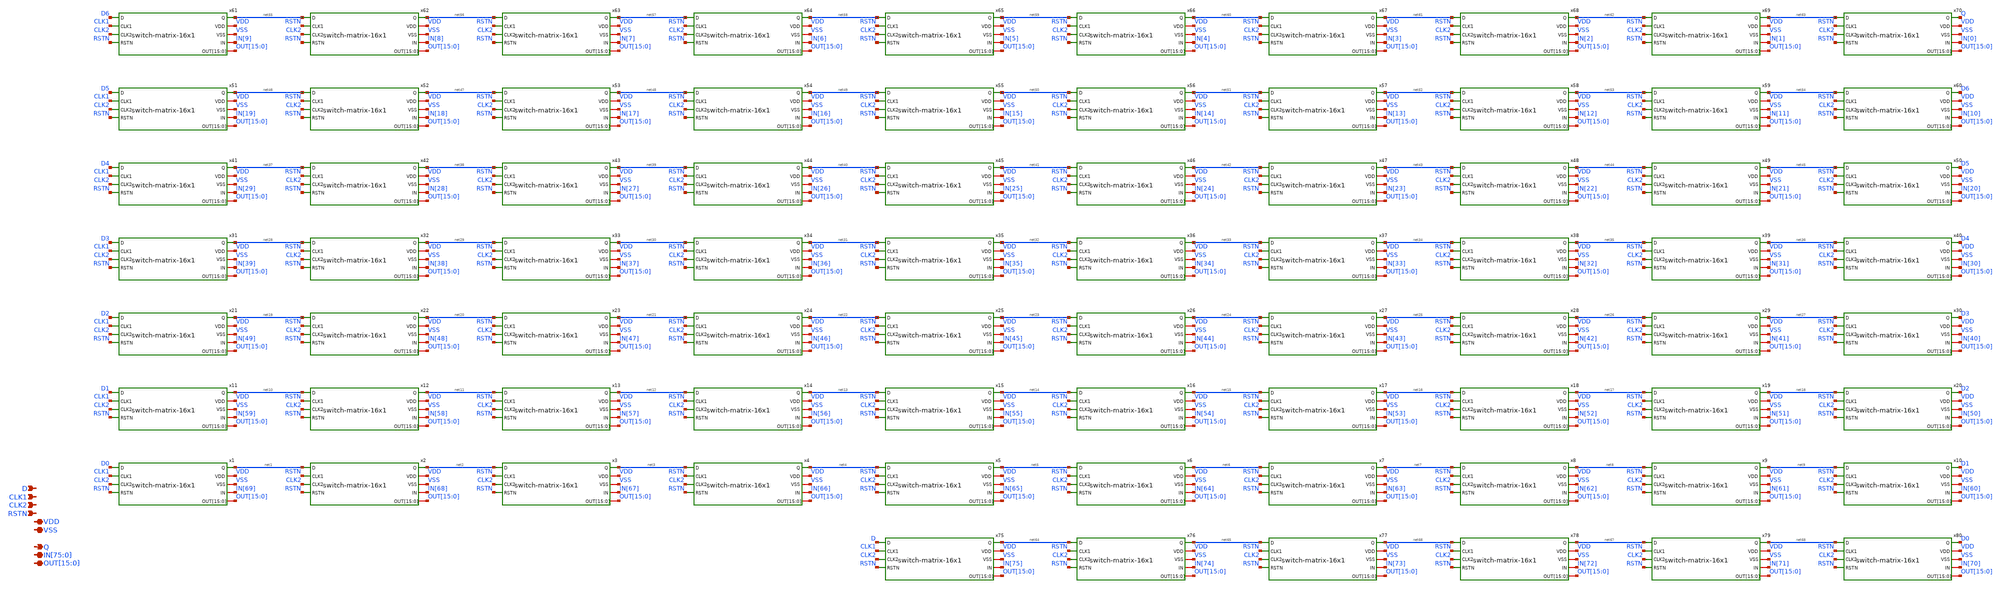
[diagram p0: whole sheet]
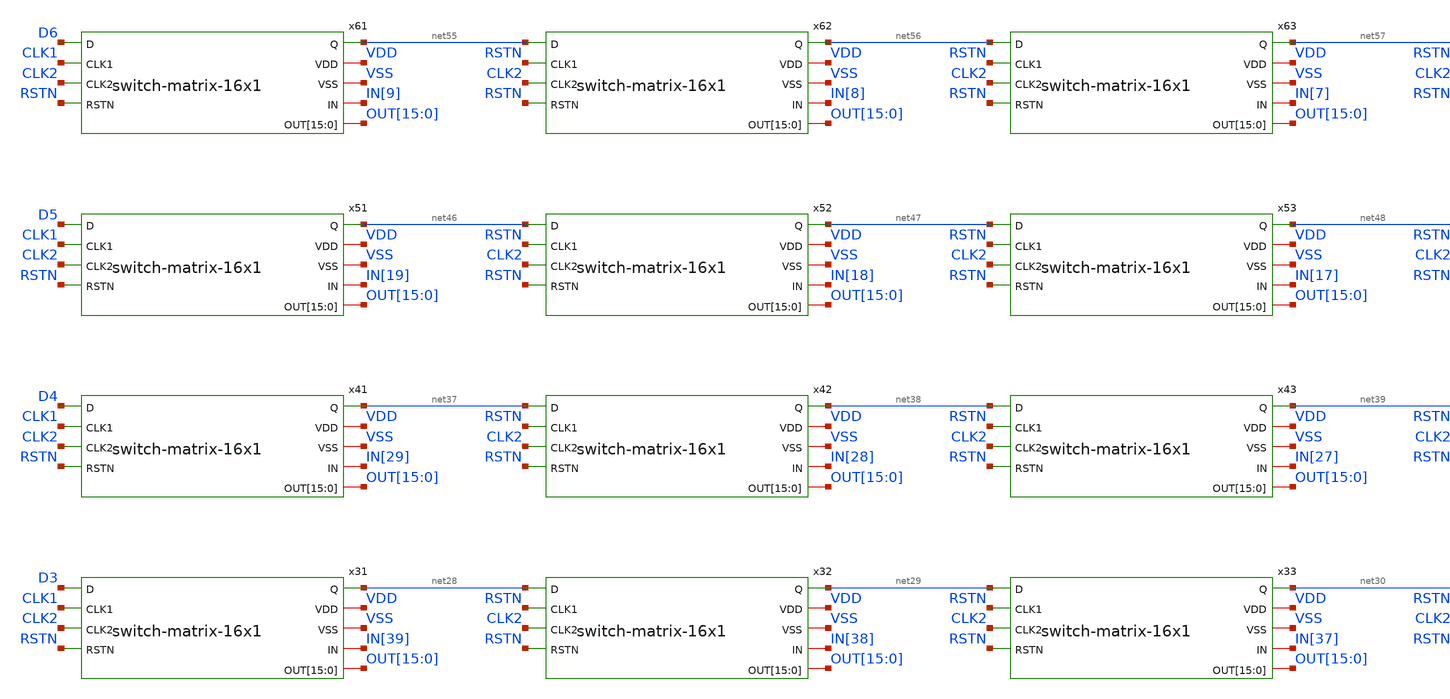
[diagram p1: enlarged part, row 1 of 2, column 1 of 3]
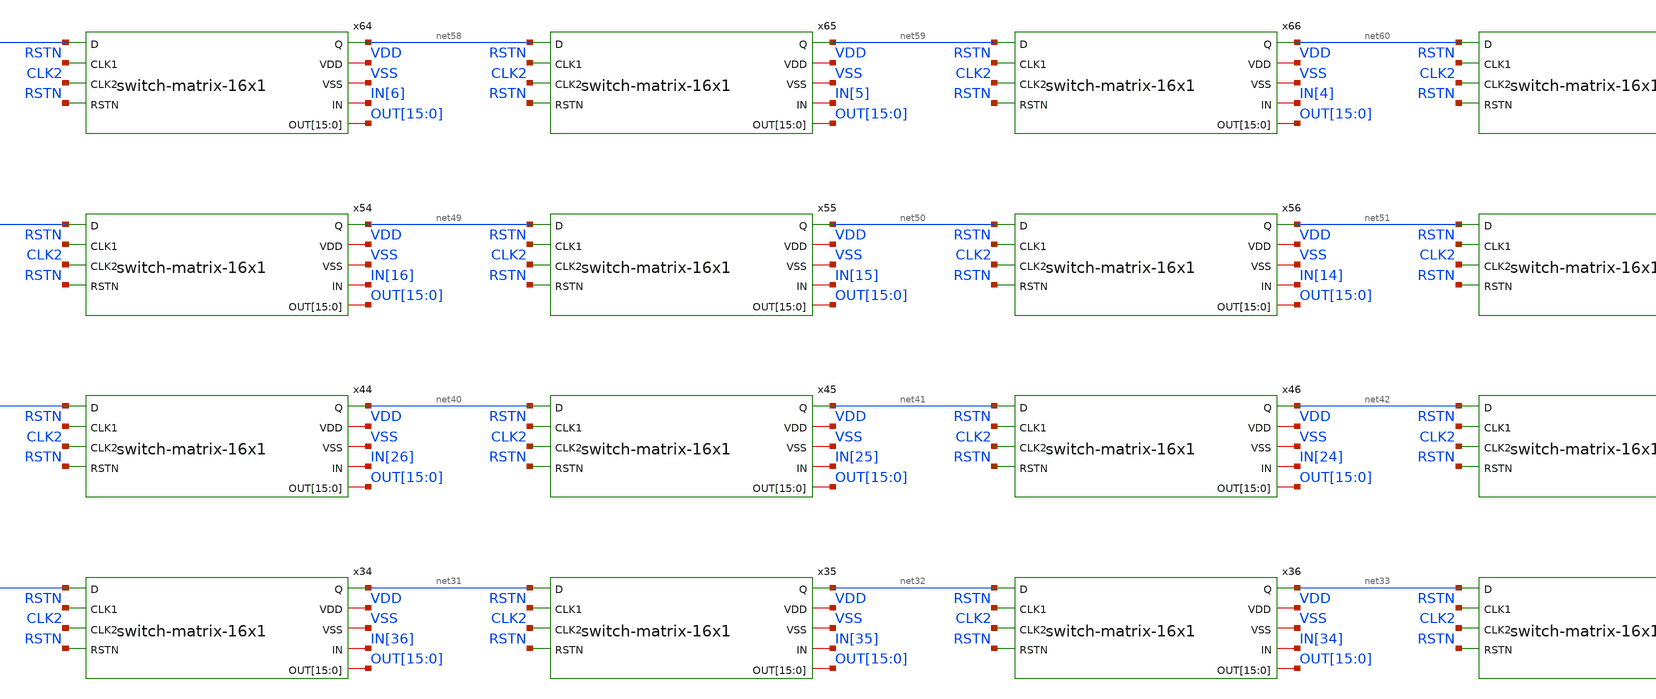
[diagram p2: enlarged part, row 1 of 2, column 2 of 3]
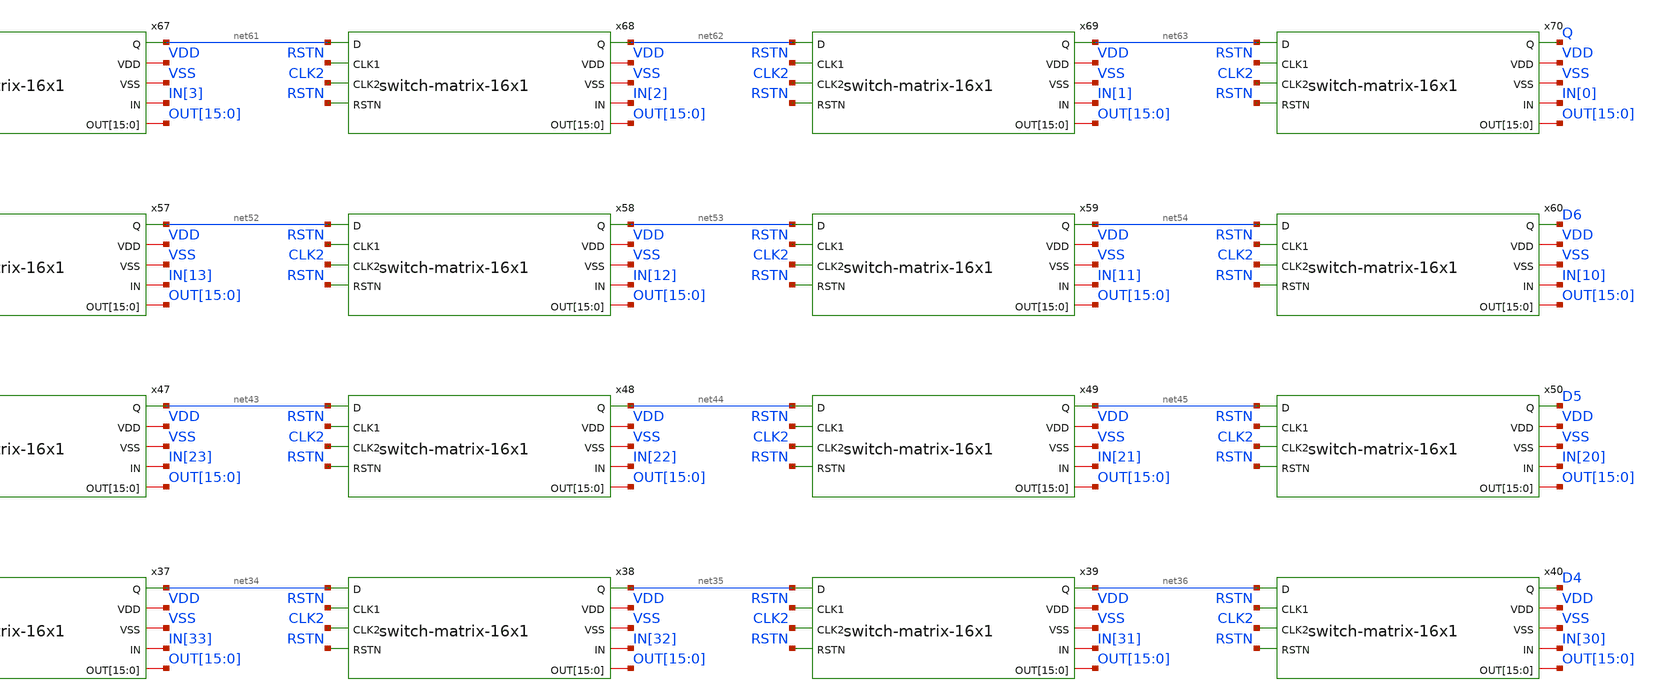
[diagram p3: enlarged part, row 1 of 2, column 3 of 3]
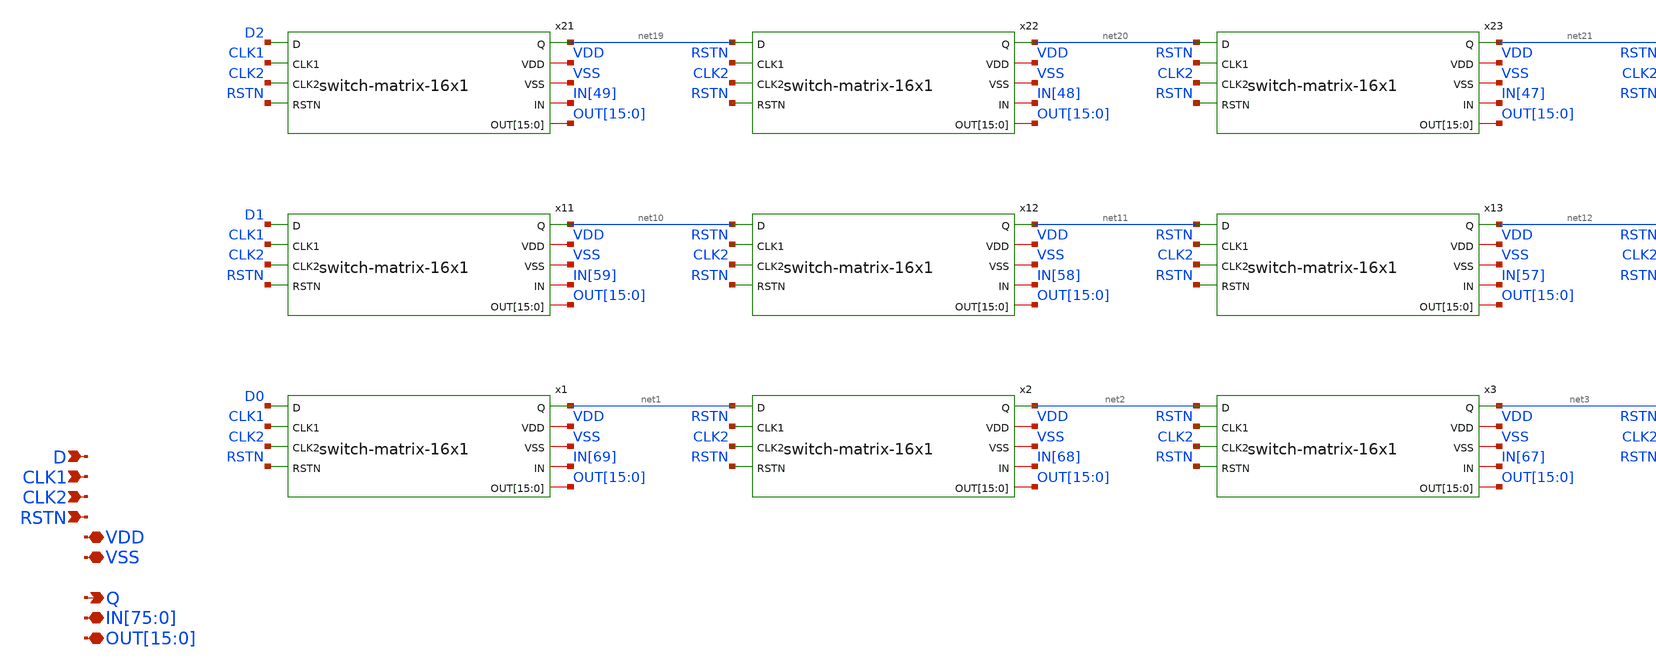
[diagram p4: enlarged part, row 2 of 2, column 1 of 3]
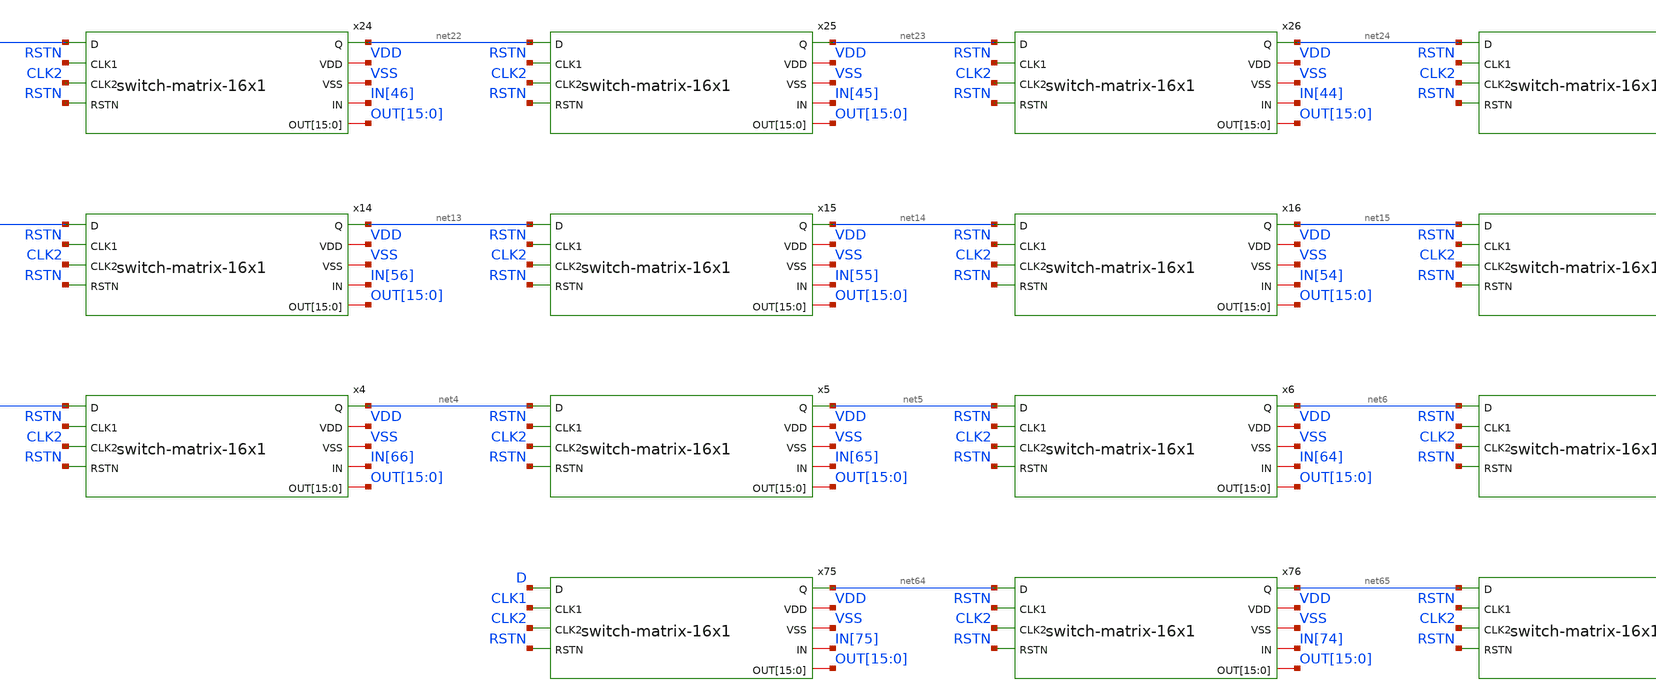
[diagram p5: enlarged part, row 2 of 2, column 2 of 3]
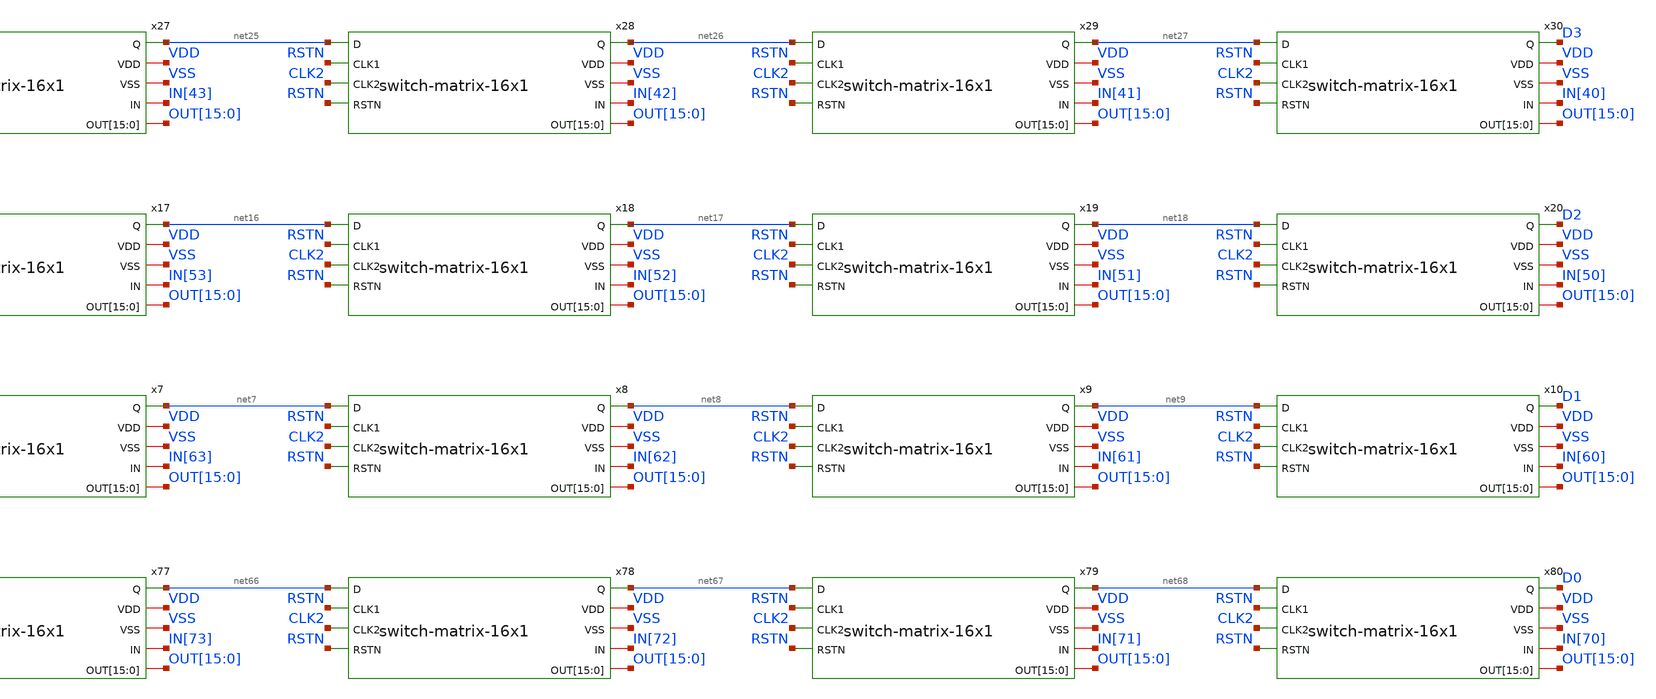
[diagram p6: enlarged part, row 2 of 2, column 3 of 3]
** sch_path: designs/libs/core_switch-matrix/switch-matrix-16x70/switch-matrix-16x70.sch
**.subckt switch-matrix-16x70 VDD VSS RSTN CLK1 CLK2 D
*+ IN[75],IN[74],IN[73],IN[72],IN[71],IN[70],IN[69],IN[68],IN[67],IN[66],IN[65],IN[64],IN[63],IN[62],IN[61],IN[60],IN[59],IN[58],IN[57],IN[56],IN[55],IN[54],IN[53],IN[52],IN[51],IN[50],IN[49],IN[48],IN[47],IN[46],IN[45],IN[44],IN[43],IN[42],IN[41],IN[40],IN[39],IN[38],IN[37],IN[36],IN[35],IN[34],IN[33],IN[32],IN[31],IN[30],IN[29],IN[28],IN[27],IN[26],IN[25],IN[24],IN[23],IN[22],IN[21],IN[20],IN[19],IN[18],IN[17],IN[16],IN[15],IN[14],IN[13],IN[12],IN[11],IN[10],IN[9],IN[8],IN[7],IN[6],IN[5],IN[4],IN[3],IN[2],IN[1],IN[0]
*+ OUT[15],OUT[14],OUT[13],OUT[12],OUT[11],OUT[10],OUT[9],OUT[8],OUT[7],OUT[6],OUT[5],OUT[4],OUT[3],OUT[2],OUT[1],OUT[0] Q
*.iopin VDD
*.iopin VSS
*.ipin RSTN
*.ipin CLK1
*.ipin CLK2
*.ipin D
*.iopin
*+ IN[75],IN[74],IN[73],IN[72],IN[71],IN[70],IN[69],IN[68],IN[67],IN[66],IN[65],IN[64],IN[63],IN[62],IN[61],IN[60],IN[59],IN[58],IN[57],IN[56],IN[55],IN[54],IN[53],IN[52],IN[51],IN[50],IN[49],IN[48],IN[47],IN[46],IN[45],IN[44],IN[43],IN[42],IN[41],IN[40],IN[39],IN[38],IN[37],IN[36],IN[35],IN[34],IN[33],IN[32],IN[31],IN[30],IN[29],IN[28],IN[27],IN[26],IN[25],IN[24],IN[23],IN[22],IN[21],IN[20],IN[19],IN[18],IN[17],IN[16],IN[15],IN[14],IN[13],IN[12],IN[11],IN[10],IN[9],IN[8],IN[7],IN[6],IN[5],IN[4],IN[3],IN[2],IN[1],IN[0]
*.iopin
*+ OUT[15],OUT[14],OUT[13],OUT[12],OUT[11],OUT[10],OUT[9],OUT[8],OUT[7],OUT[6],OUT[5],OUT[4],OUT[3],OUT[2],OUT[1],OUT[0]
*.opin Q
x1 net1 VDD VSS IN[69] OUT[15] OUT[14] OUT[13] OUT[12] OUT[11] OUT[10] OUT[9] OUT[8] OUT[7] OUT[6]
+ OUT[5] OUT[4] OUT[3] OUT[2] OUT[1] OUT[0] D0 CLK1 CLK2 RSTN switch-matrix-16x1
x2 net2 VDD VSS IN[68] OUT[15] OUT[14] OUT[13] OUT[12] OUT[11] OUT[10] OUT[9] OUT[8] OUT[7] OUT[6]
+ OUT[5] OUT[4] OUT[3] OUT[2] OUT[1] OUT[0] net1 RSTN CLK2 RSTN switch-matrix-16x1
x3 net3 VDD VSS IN[67] OUT[15] OUT[14] OUT[13] OUT[12] OUT[11] OUT[10] OUT[9] OUT[8] OUT[7] OUT[6]
+ OUT[5] OUT[4] OUT[3] OUT[2] OUT[1] OUT[0] net2 RSTN CLK2 RSTN switch-matrix-16x1
x4 net4 VDD VSS IN[66] OUT[15] OUT[14] OUT[13] OUT[12] OUT[11] OUT[10] OUT[9] OUT[8] OUT[7] OUT[6]
+ OUT[5] OUT[4] OUT[3] OUT[2] OUT[1] OUT[0] net3 RSTN CLK2 RSTN switch-matrix-16x1
x5 net5 VDD VSS IN[65] OUT[15] OUT[14] OUT[13] OUT[12] OUT[11] OUT[10] OUT[9] OUT[8] OUT[7] OUT[6]
+ OUT[5] OUT[4] OUT[3] OUT[2] OUT[1] OUT[0] net4 RSTN CLK2 RSTN switch-matrix-16x1
x6 net6 VDD VSS IN[64] OUT[15] OUT[14] OUT[13] OUT[12] OUT[11] OUT[10] OUT[9] OUT[8] OUT[7] OUT[6]
+ OUT[5] OUT[4] OUT[3] OUT[2] OUT[1] OUT[0] net5 RSTN CLK2 RSTN switch-matrix-16x1
x7 net7 VDD VSS IN[63] OUT[15] OUT[14] OUT[13] OUT[12] OUT[11] OUT[10] OUT[9] OUT[8] OUT[7] OUT[6]
+ OUT[5] OUT[4] OUT[3] OUT[2] OUT[1] OUT[0] net6 RSTN CLK2 RSTN switch-matrix-16x1
x8 net8 VDD VSS IN[62] OUT[15] OUT[14] OUT[13] OUT[12] OUT[11] OUT[10] OUT[9] OUT[8] OUT[7] OUT[6]
+ OUT[5] OUT[4] OUT[3] OUT[2] OUT[1] OUT[0] net7 RSTN CLK2 RSTN switch-matrix-16x1
x9 net9 VDD VSS IN[61] OUT[15] OUT[14] OUT[13] OUT[12] OUT[11] OUT[10] OUT[9] OUT[8] OUT[7] OUT[6]
+ OUT[5] OUT[4] OUT[3] OUT[2] OUT[1] OUT[0] net8 RSTN CLK2 RSTN switch-matrix-16x1
x10 D1 VDD VSS IN[60] OUT[15] OUT[14] OUT[13] OUT[12] OUT[11] OUT[10] OUT[9] OUT[8] OUT[7] OUT[6]
+ OUT[5] OUT[4] OUT[3] OUT[2] OUT[1] OUT[0] net9 RSTN CLK2 RSTN switch-matrix-16x1
x11 net10 VDD VSS IN[59] OUT[15] OUT[14] OUT[13] OUT[12] OUT[11] OUT[10] OUT[9] OUT[8] OUT[7] OUT[6]
+ OUT[5] OUT[4] OUT[3] OUT[2] OUT[1] OUT[0] D1 CLK1 CLK2 RSTN switch-matrix-16x1
x12 net11 VDD VSS IN[58] OUT[15] OUT[14] OUT[13] OUT[12] OUT[11] OUT[10] OUT[9] OUT[8] OUT[7] OUT[6]
+ OUT[5] OUT[4] OUT[3] OUT[2] OUT[1] OUT[0] net10 RSTN CLK2 RSTN switch-matrix-16x1
x13 net12 VDD VSS IN[57] OUT[15] OUT[14] OUT[13] OUT[12] OUT[11] OUT[10] OUT[9] OUT[8] OUT[7] OUT[6]
+ OUT[5] OUT[4] OUT[3] OUT[2] OUT[1] OUT[0] net11 RSTN CLK2 RSTN switch-matrix-16x1
x14 net13 VDD VSS IN[56] OUT[15] OUT[14] OUT[13] OUT[12] OUT[11] OUT[10] OUT[9] OUT[8] OUT[7] OUT[6]
+ OUT[5] OUT[4] OUT[3] OUT[2] OUT[1] OUT[0] net12 RSTN CLK2 RSTN switch-matrix-16x1
x15 net14 VDD VSS IN[55] OUT[15] OUT[14] OUT[13] OUT[12] OUT[11] OUT[10] OUT[9] OUT[8] OUT[7] OUT[6]
+ OUT[5] OUT[4] OUT[3] OUT[2] OUT[1] OUT[0] net13 RSTN CLK2 RSTN switch-matrix-16x1
x16 net15 VDD VSS IN[54] OUT[15] OUT[14] OUT[13] OUT[12] OUT[11] OUT[10] OUT[9] OUT[8] OUT[7] OUT[6]
+ OUT[5] OUT[4] OUT[3] OUT[2] OUT[1] OUT[0] net14 RSTN CLK2 RSTN switch-matrix-16x1
x17 net16 VDD VSS IN[53] OUT[15] OUT[14] OUT[13] OUT[12] OUT[11] OUT[10] OUT[9] OUT[8] OUT[7] OUT[6]
+ OUT[5] OUT[4] OUT[3] OUT[2] OUT[1] OUT[0] net15 RSTN CLK2 RSTN switch-matrix-16x1
x18 net17 VDD VSS IN[52] OUT[15] OUT[14] OUT[13] OUT[12] OUT[11] OUT[10] OUT[9] OUT[8] OUT[7] OUT[6]
+ OUT[5] OUT[4] OUT[3] OUT[2] OUT[1] OUT[0] net16 RSTN CLK2 RSTN switch-matrix-16x1
x19 net18 VDD VSS IN[51] OUT[15] OUT[14] OUT[13] OUT[12] OUT[11] OUT[10] OUT[9] OUT[8] OUT[7] OUT[6]
+ OUT[5] OUT[4] OUT[3] OUT[2] OUT[1] OUT[0] net17 RSTN CLK2 RSTN switch-matrix-16x1
x20 D2 VDD VSS IN[50] OUT[15] OUT[14] OUT[13] OUT[12] OUT[11] OUT[10] OUT[9] OUT[8] OUT[7] OUT[6]
+ OUT[5] OUT[4] OUT[3] OUT[2] OUT[1] OUT[0] net18 RSTN CLK2 RSTN switch-matrix-16x1
x21 net19 VDD VSS IN[49] OUT[15] OUT[14] OUT[13] OUT[12] OUT[11] OUT[10] OUT[9] OUT[8] OUT[7] OUT[6]
+ OUT[5] OUT[4] OUT[3] OUT[2] OUT[1] OUT[0] D2 CLK1 CLK2 RSTN switch-matrix-16x1
x22 net20 VDD VSS IN[48] OUT[15] OUT[14] OUT[13] OUT[12] OUT[11] OUT[10] OUT[9] OUT[8] OUT[7] OUT[6]
+ OUT[5] OUT[4] OUT[3] OUT[2] OUT[1] OUT[0] net19 RSTN CLK2 RSTN switch-matrix-16x1
x23 net21 VDD VSS IN[47] OUT[15] OUT[14] OUT[13] OUT[12] OUT[11] OUT[10] OUT[9] OUT[8] OUT[7] OUT[6]
+ OUT[5] OUT[4] OUT[3] OUT[2] OUT[1] OUT[0] net20 RSTN CLK2 RSTN switch-matrix-16x1
x24 net22 VDD VSS IN[46] OUT[15] OUT[14] OUT[13] OUT[12] OUT[11] OUT[10] OUT[9] OUT[8] OUT[7] OUT[6]
+ OUT[5] OUT[4] OUT[3] OUT[2] OUT[1] OUT[0] net21 RSTN CLK2 RSTN switch-matrix-16x1
x25 net23 VDD VSS IN[45] OUT[15] OUT[14] OUT[13] OUT[12] OUT[11] OUT[10] OUT[9] OUT[8] OUT[7] OUT[6]
+ OUT[5] OUT[4] OUT[3] OUT[2] OUT[1] OUT[0] net22 RSTN CLK2 RSTN switch-matrix-16x1
x26 net24 VDD VSS IN[44] OUT[15] OUT[14] OUT[13] OUT[12] OUT[11] OUT[10] OUT[9] OUT[8] OUT[7] OUT[6]
+ OUT[5] OUT[4] OUT[3] OUT[2] OUT[1] OUT[0] net23 RSTN CLK2 RSTN switch-matrix-16x1
x27 net25 VDD VSS IN[43] OUT[15] OUT[14] OUT[13] OUT[12] OUT[11] OUT[10] OUT[9] OUT[8] OUT[7] OUT[6]
+ OUT[5] OUT[4] OUT[3] OUT[2] OUT[1] OUT[0] net24 RSTN CLK2 RSTN switch-matrix-16x1
x28 net26 VDD VSS IN[42] OUT[15] OUT[14] OUT[13] OUT[12] OUT[11] OUT[10] OUT[9] OUT[8] OUT[7] OUT[6]
+ OUT[5] OUT[4] OUT[3] OUT[2] OUT[1] OUT[0] net25 RSTN CLK2 RSTN switch-matrix-16x1
x29 net27 VDD VSS IN[41] OUT[15] OUT[14] OUT[13] OUT[12] OUT[11] OUT[10] OUT[9] OUT[8] OUT[7] OUT[6]
+ OUT[5] OUT[4] OUT[3] OUT[2] OUT[1] OUT[0] net26 RSTN CLK2 RSTN switch-matrix-16x1
x30 D3 VDD VSS IN[40] OUT[15] OUT[14] OUT[13] OUT[12] OUT[11] OUT[10] OUT[9] OUT[8] OUT[7] OUT[6]
+ OUT[5] OUT[4] OUT[3] OUT[2] OUT[1] OUT[0] net27 RSTN CLK2 RSTN switch-matrix-16x1
x31 net28 VDD VSS IN[39] OUT[15] OUT[14] OUT[13] OUT[12] OUT[11] OUT[10] OUT[9] OUT[8] OUT[7] OUT[6]
+ OUT[5] OUT[4] OUT[3] OUT[2] OUT[1] OUT[0] D3 CLK1 CLK2 RSTN switch-matrix-16x1
x32 net29 VDD VSS IN[38] OUT[15] OUT[14] OUT[13] OUT[12] OUT[11] OUT[10] OUT[9] OUT[8] OUT[7] OUT[6]
+ OUT[5] OUT[4] OUT[3] OUT[2] OUT[1] OUT[0] net28 RSTN CLK2 RSTN switch-matrix-16x1
x33 net30 VDD VSS IN[37] OUT[15] OUT[14] OUT[13] OUT[12] OUT[11] OUT[10] OUT[9] OUT[8] OUT[7] OUT[6]
+ OUT[5] OUT[4] OUT[3] OUT[2] OUT[1] OUT[0] net29 RSTN CLK2 RSTN switch-matrix-16x1
x34 net31 VDD VSS IN[36] OUT[15] OUT[14] OUT[13] OUT[12] OUT[11] OUT[10] OUT[9] OUT[8] OUT[7] OUT[6]
+ OUT[5] OUT[4] OUT[3] OUT[2] OUT[1] OUT[0] net30 RSTN CLK2 RSTN switch-matrix-16x1
x35 net32 VDD VSS IN[35] OUT[15] OUT[14] OUT[13] OUT[12] OUT[11] OUT[10] OUT[9] OUT[8] OUT[7] OUT[6]
+ OUT[5] OUT[4] OUT[3] OUT[2] OUT[1] OUT[0] net31 RSTN CLK2 RSTN switch-matrix-16x1
x36 net33 VDD VSS IN[34] OUT[15] OUT[14] OUT[13] OUT[12] OUT[11] OUT[10] OUT[9] OUT[8] OUT[7] OUT[6]
+ OUT[5] OUT[4] OUT[3] OUT[2] OUT[1] OUT[0] net32 RSTN CLK2 RSTN switch-matrix-16x1
x37 net34 VDD VSS IN[33] OUT[15] OUT[14] OUT[13] OUT[12] OUT[11] OUT[10] OUT[9] OUT[8] OUT[7] OUT[6]
+ OUT[5] OUT[4] OUT[3] OUT[2] OUT[1] OUT[0] net33 RSTN CLK2 RSTN switch-matrix-16x1
x38 net35 VDD VSS IN[32] OUT[15] OUT[14] OUT[13] OUT[12] OUT[11] OUT[10] OUT[9] OUT[8] OUT[7] OUT[6]
+ OUT[5] OUT[4] OUT[3] OUT[2] OUT[1] OUT[0] net34 RSTN CLK2 RSTN switch-matrix-16x1
x39 net36 VDD VSS IN[31] OUT[15] OUT[14] OUT[13] OUT[12] OUT[11] OUT[10] OUT[9] OUT[8] OUT[7] OUT[6]
+ OUT[5] OUT[4] OUT[3] OUT[2] OUT[1] OUT[0] net35 RSTN CLK2 RSTN switch-matrix-16x1
x40 D4 VDD VSS IN[30] OUT[15] OUT[14] OUT[13] OUT[12] OUT[11] OUT[10] OUT[9] OUT[8] OUT[7] OUT[6]
+ OUT[5] OUT[4] OUT[3] OUT[2] OUT[1] OUT[0] net36 RSTN CLK2 RSTN switch-matrix-16x1
x41 net37 VDD VSS IN[29] OUT[15] OUT[14] OUT[13] OUT[12] OUT[11] OUT[10] OUT[9] OUT[8] OUT[7] OUT[6]
+ OUT[5] OUT[4] OUT[3] OUT[2] OUT[1] OUT[0] D4 CLK1 CLK2 RSTN switch-matrix-16x1
x42 net38 VDD VSS IN[28] OUT[15] OUT[14] OUT[13] OUT[12] OUT[11] OUT[10] OUT[9] OUT[8] OUT[7] OUT[6]
+ OUT[5] OUT[4] OUT[3] OUT[2] OUT[1] OUT[0] net37 RSTN CLK2 RSTN switch-matrix-16x1
x43 net39 VDD VSS IN[27] OUT[15] OUT[14] OUT[13] OUT[12] OUT[11] OUT[10] OUT[9] OUT[8] OUT[7] OUT[6]
+ OUT[5] OUT[4] OUT[3] OUT[2] OUT[1] OUT[0] net38 RSTN CLK2 RSTN switch-matrix-16x1
x44 net40 VDD VSS IN[26] OUT[15] OUT[14] OUT[13] OUT[12] OUT[11] OUT[10] OUT[9] OUT[8] OUT[7] OUT[6]
+ OUT[5] OUT[4] OUT[3] OUT[2] OUT[1] OUT[0] net39 RSTN CLK2 RSTN switch-matrix-16x1
x45 net41 VDD VSS IN[25] OUT[15] OUT[14] OUT[13] OUT[12] OUT[11] OUT[10] OUT[9] OUT[8] OUT[7] OUT[6]
+ OUT[5] OUT[4] OUT[3] OUT[2] OUT[1] OUT[0] net40 RSTN CLK2 RSTN switch-matrix-16x1
x46 net42 VDD VSS IN[24] OUT[15] OUT[14] OUT[13] OUT[12] OUT[11] OUT[10] OUT[9] OUT[8] OUT[7] OUT[6]
+ OUT[5] OUT[4] OUT[3] OUT[2] OUT[1] OUT[0] net41 RSTN CLK2 RSTN switch-matrix-16x1
x47 net43 VDD VSS IN[23] OUT[15] OUT[14] OUT[13] OUT[12] OUT[11] OUT[10] OUT[9] OUT[8] OUT[7] OUT[6]
+ OUT[5] OUT[4] OUT[3] OUT[2] OUT[1] OUT[0] net42 RSTN CLK2 RSTN switch-matrix-16x1
x48 net44 VDD VSS IN[22] OUT[15] OUT[14] OUT[13] OUT[12] OUT[11] OUT[10] OUT[9] OUT[8] OUT[7] OUT[6]
+ OUT[5] OUT[4] OUT[3] OUT[2] OUT[1] OUT[0] net43 RSTN CLK2 RSTN switch-matrix-16x1
x49 net45 VDD VSS IN[21] OUT[15] OUT[14] OUT[13] OUT[12] OUT[11] OUT[10] OUT[9] OUT[8] OUT[7] OUT[6]
+ OUT[5] OUT[4] OUT[3] OUT[2] OUT[1] OUT[0] net44 RSTN CLK2 RSTN switch-matrix-16x1
x50 D5 VDD VSS IN[20] OUT[15] OUT[14] OUT[13] OUT[12] OUT[11] OUT[10] OUT[9] OUT[8] OUT[7] OUT[6]
+ OUT[5] OUT[4] OUT[3] OUT[2] OUT[1] OUT[0] net45 RSTN CLK2 RSTN switch-matrix-16x1
x51 net46 VDD VSS IN[19] OUT[15] OUT[14] OUT[13] OUT[12] OUT[11] OUT[10] OUT[9] OUT[8] OUT[7] OUT[6]
+ OUT[5] OUT[4] OUT[3] OUT[2] OUT[1] OUT[0] D5 CLK1 CLK2 RSTN switch-matrix-16x1
x52 net47 VDD VSS IN[18] OUT[15] OUT[14] OUT[13] OUT[12] OUT[11] OUT[10] OUT[9] OUT[8] OUT[7] OUT[6]
+ OUT[5] OUT[4] OUT[3] OUT[2] OUT[1] OUT[0] net46 RSTN CLK2 RSTN switch-matrix-16x1
x53 net48 VDD VSS IN[17] OUT[15] OUT[14] OUT[13] OUT[12] OUT[11] OUT[10] OUT[9] OUT[8] OUT[7] OUT[6]
+ OUT[5] OUT[4] OUT[3] OUT[2] OUT[1] OUT[0] net47 RSTN CLK2 RSTN switch-matrix-16x1
x54 net49 VDD VSS IN[16] OUT[15] OUT[14] OUT[13] OUT[12] OUT[11] OUT[10] OUT[9] OUT[8] OUT[7] OUT[6]
+ OUT[5] OUT[4] OUT[3] OUT[2] OUT[1] OUT[0] net48 RSTN CLK2 RSTN switch-matrix-16x1
x55 net50 VDD VSS IN[15] OUT[15] OUT[14] OUT[13] OUT[12] OUT[11] OUT[10] OUT[9] OUT[8] OUT[7] OUT[6]
+ OUT[5] OUT[4] OUT[3] OUT[2] OUT[1] OUT[0] net49 RSTN CLK2 RSTN switch-matrix-16x1
x56 net51 VDD VSS IN[14] OUT[15] OUT[14] OUT[13] OUT[12] OUT[11] OUT[10] OUT[9] OUT[8] OUT[7] OUT[6]
+ OUT[5] OUT[4] OUT[3] OUT[2] OUT[1] OUT[0] net50 RSTN CLK2 RSTN switch-matrix-16x1
x57 net52 VDD VSS IN[13] OUT[15] OUT[14] OUT[13] OUT[12] OUT[11] OUT[10] OUT[9] OUT[8] OUT[7] OUT[6]
+ OUT[5] OUT[4] OUT[3] OUT[2] OUT[1] OUT[0] net51 RSTN CLK2 RSTN switch-matrix-16x1
x58 net53 VDD VSS IN[12] OUT[15] OUT[14] OUT[13] OUT[12] OUT[11] OUT[10] OUT[9] OUT[8] OUT[7] OUT[6]
+ OUT[5] OUT[4] OUT[3] OUT[2] OUT[1] OUT[0] net52 RSTN CLK2 RSTN switch-matrix-16x1
x59 net54 VDD VSS IN[11] OUT[15] OUT[14] OUT[13] OUT[12] OUT[11] OUT[10] OUT[9] OUT[8] OUT[7] OUT[6]
+ OUT[5] OUT[4] OUT[3] OUT[2] OUT[1] OUT[0] net53 RSTN CLK2 RSTN switch-matrix-16x1
x60 D6 VDD VSS IN[10] OUT[15] OUT[14] OUT[13] OUT[12] OUT[11] OUT[10] OUT[9] OUT[8] OUT[7] OUT[6]
+ OUT[5] OUT[4] OUT[3] OUT[2] OUT[1] OUT[0] net54 RSTN CLK2 RSTN switch-matrix-16x1
x61 net55 VDD VSS IN[9] OUT[15] OUT[14] OUT[13] OUT[12] OUT[11] OUT[10] OUT[9] OUT[8] OUT[7] OUT[6]
+ OUT[5] OUT[4] OUT[3] OUT[2] OUT[1] OUT[0] D6 CLK1 CLK2 RSTN switch-matrix-16x1
x62 net56 VDD VSS IN[8] OUT[15] OUT[14] OUT[13] OUT[12] OUT[11] OUT[10] OUT[9] OUT[8] OUT[7] OUT[6]
+ OUT[5] OUT[4] OUT[3] OUT[2] OUT[1] OUT[0] net55 RSTN CLK2 RSTN switch-matrix-16x1
x63 net57 VDD VSS IN[7] OUT[15] OUT[14] OUT[13] OUT[12] OUT[11] OUT[10] OUT[9] OUT[8] OUT[7] OUT[6]
+ OUT[5] OUT[4] OUT[3] OUT[2] OUT[1] OUT[0] net56 RSTN CLK2 RSTN switch-matrix-16x1
x64 net58 VDD VSS IN[6] OUT[15] OUT[14] OUT[13] OUT[12] OUT[11] OUT[10] OUT[9] OUT[8] OUT[7] OUT[6]
+ OUT[5] OUT[4] OUT[3] OUT[2] OUT[1] OUT[0] net57 RSTN CLK2 RSTN switch-matrix-16x1
x65 net59 VDD VSS IN[5] OUT[15] OUT[14] OUT[13] OUT[12] OUT[11] OUT[10] OUT[9] OUT[8] OUT[7] OUT[6]
+ OUT[5] OUT[4] OUT[3] OUT[2] OUT[1] OUT[0] net58 RSTN CLK2 RSTN switch-matrix-16x1
x66 net60 VDD VSS IN[4] OUT[15] OUT[14] OUT[13] OUT[12] OUT[11] OUT[10] OUT[9] OUT[8] OUT[7] OUT[6]
+ OUT[5] OUT[4] OUT[3] OUT[2] OUT[1] OUT[0] net59 RSTN CLK2 RSTN switch-matrix-16x1
x67 net61 VDD VSS IN[3] OUT[15] OUT[14] OUT[13] OUT[12] OUT[11] OUT[10] OUT[9] OUT[8] OUT[7] OUT[6]
+ OUT[5] OUT[4] OUT[3] OUT[2] OUT[1] OUT[0] net60 RSTN CLK2 RSTN switch-matrix-16x1
x68 net62 VDD VSS IN[2] OUT[15] OUT[14] OUT[13] OUT[12] OUT[11] OUT[10] OUT[9] OUT[8] OUT[7] OUT[6]
+ OUT[5] OUT[4] OUT[3] OUT[2] OUT[1] OUT[0] net61 RSTN CLK2 RSTN switch-matrix-16x1
x69 net63 VDD VSS IN[1] OUT[15] OUT[14] OUT[13] OUT[12] OUT[11] OUT[10] OUT[9] OUT[8] OUT[7] OUT[6]
+ OUT[5] OUT[4] OUT[3] OUT[2] OUT[1] OUT[0] net62 RSTN CLK2 RSTN switch-matrix-16x1
x70 Q VDD VSS IN[0] OUT[15] OUT[14] OUT[13] OUT[12] OUT[11] OUT[10] OUT[9] OUT[8] OUT[7] OUT[6]
+ OUT[5] OUT[4] OUT[3] OUT[2] OUT[1] OUT[0] net63 RSTN CLK2 RSTN switch-matrix-16x1
x75 net64 VDD VSS IN[75] OUT[15] OUT[14] OUT[13] OUT[12] OUT[11] OUT[10] OUT[9] OUT[8] OUT[7] OUT[6]
+ OUT[5] OUT[4] OUT[3] OUT[2] OUT[1] OUT[0] D CLK1 CLK2 RSTN switch-matrix-16x1
x76 net65 VDD VSS IN[74] OUT[15] OUT[14] OUT[13] OUT[12] OUT[11] OUT[10] OUT[9] OUT[8] OUT[7] OUT[6]
+ OUT[5] OUT[4] OUT[3] OUT[2] OUT[1] OUT[0] net64 RSTN CLK2 RSTN switch-matrix-16x1
x77 net66 VDD VSS IN[73] OUT[15] OUT[14] OUT[13] OUT[12] OUT[11] OUT[10] OUT[9] OUT[8] OUT[7] OUT[6]
+ OUT[5] OUT[4] OUT[3] OUT[2] OUT[1] OUT[0] net65 RSTN CLK2 RSTN switch-matrix-16x1
x78 net67 VDD VSS IN[72] OUT[15] OUT[14] OUT[13] OUT[12] OUT[11] OUT[10] OUT[9] OUT[8] OUT[7] OUT[6]
+ OUT[5] OUT[4] OUT[3] OUT[2] OUT[1] OUT[0] net66 RSTN CLK2 RSTN switch-matrix-16x1
x79 net68 VDD VSS IN[71] OUT[15] OUT[14] OUT[13] OUT[12] OUT[11] OUT[10] OUT[9] OUT[8] OUT[7] OUT[6]
+ OUT[5] OUT[4] OUT[3] OUT[2] OUT[1] OUT[0] net67 RSTN CLK2 RSTN switch-matrix-16x1
x80 D0 VDD VSS IN[70] OUT[15] OUT[14] OUT[13] OUT[12] OUT[11] OUT[10] OUT[9] OUT[8] OUT[7] OUT[6]
+ OUT[5] OUT[4] OUT[3] OUT[2] OUT[1] OUT[0] net68 RSTN CLK2 RSTN switch-matrix-16x1
**.ends
.end
